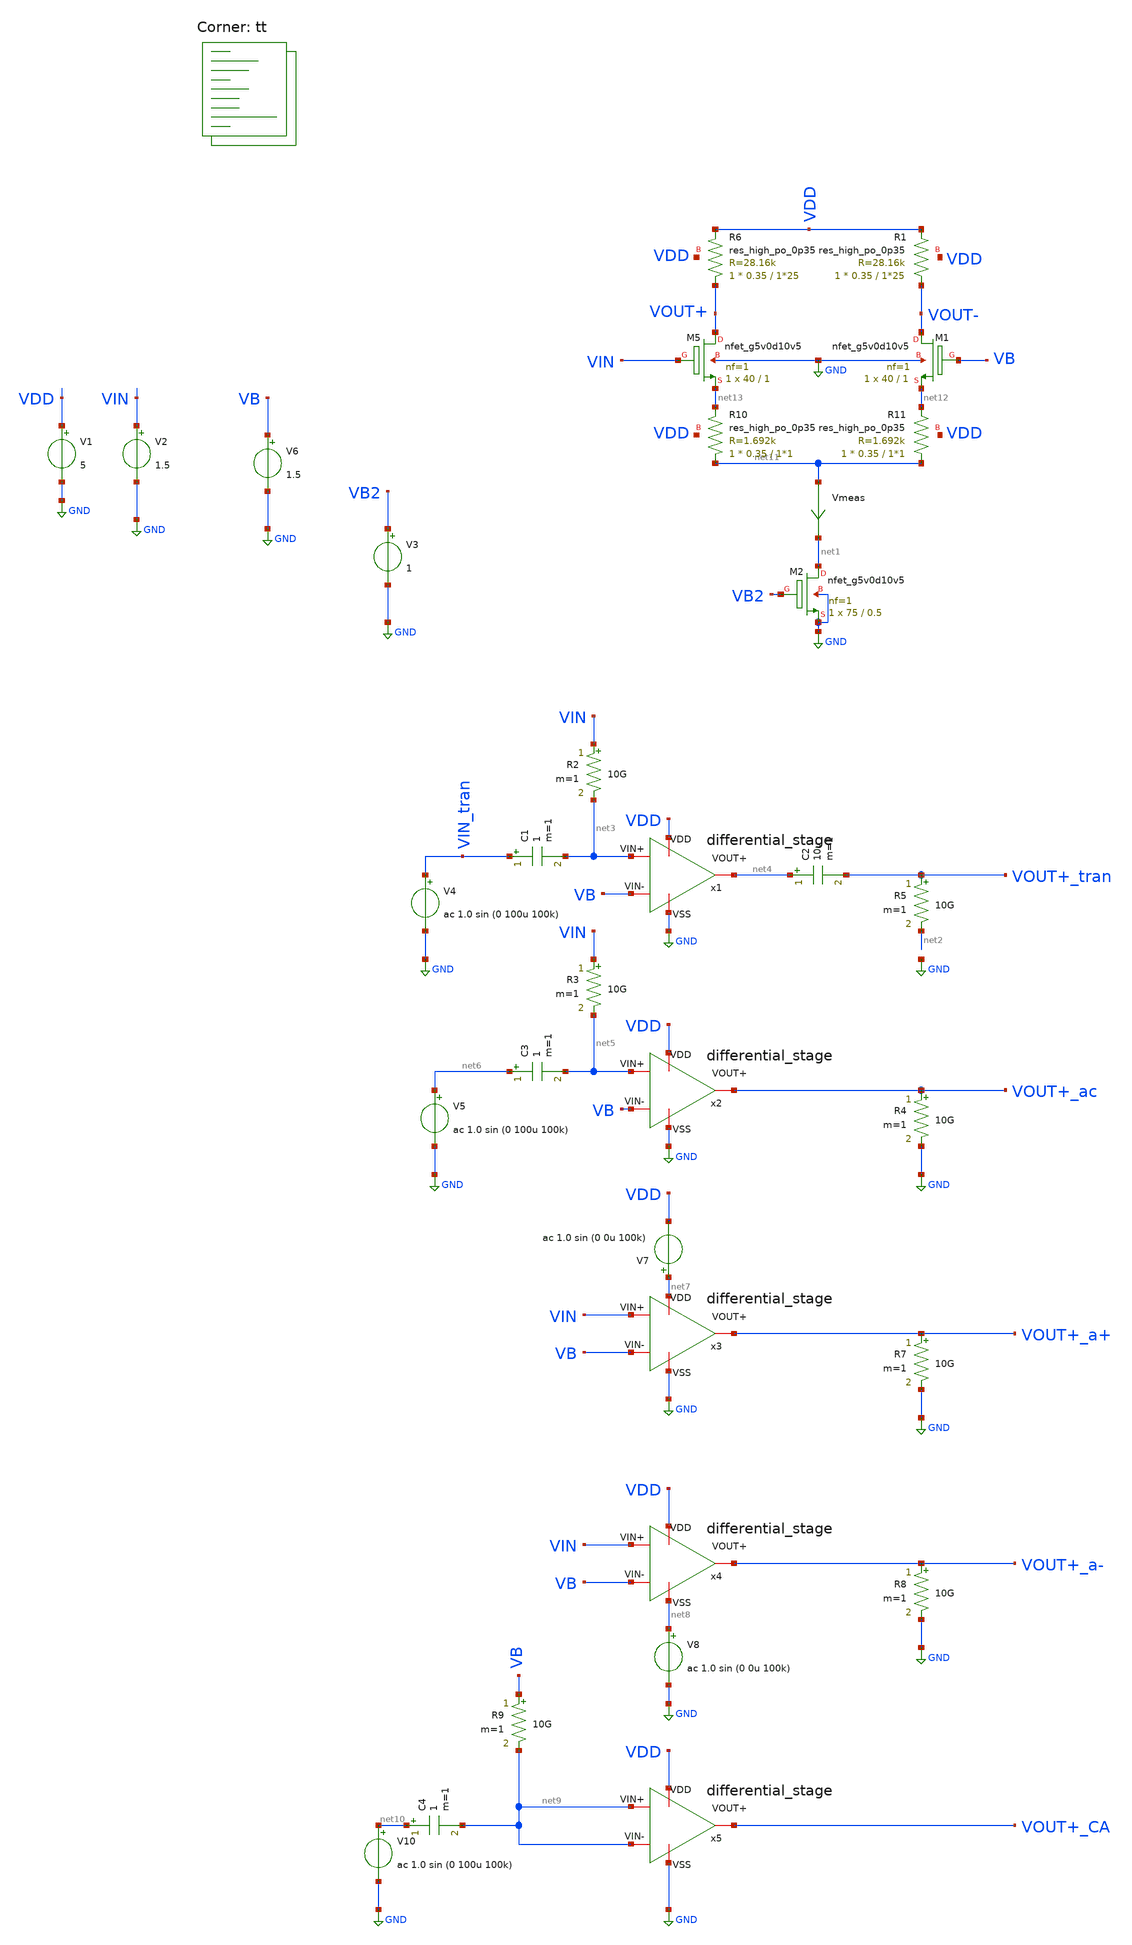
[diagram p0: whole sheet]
** sch_path: amplifiers/differencial_stage_amps/basic_stages/degenerated_stage/diferential_stage.sch
**.subckt diferential_stage
XM5 VOUT+ VIN net13 GND sky130_fd_pr__nfet_g5v0d10v5 L=1 W=40 nf=1 ad='int((1 + 1)/2) * 40 / 1 * 0.29'
+ as='int((1 + 2)/2) * 40 / 1 * 0.29' pd='2*int((1 + 1)/2) * (40 / 1 + 0.29)' ps='2*int((1 + 2)/2) * (40 / 1 + 0.29)'
+ nrd='0.29 / 40 ' nrs='0.29 / 40 ' sa=0 sb=0 sd=0 mult=1 m=1
XM1 VOUT- VB net12 GND sky130_fd_pr__nfet_g5v0d10v5 L=1 W=40 nf=1 ad='int((1 + 1)/2) * 40 / 1 * 0.29'
+ as='int((1 + 2)/2) * 40 / 1 * 0.29' pd='2*int((1 + 1)/2) * (40 / 1 + 0.29)' ps='2*int((1 + 2)/2) * (40 / 1 + 0.29)'
+ nrd='0.29 / 40 ' nrs='0.29 / 40 ' sa=0 sb=0 sd=0 mult=1 m=1
XR6 VOUT+ VDD VDD sky130_fd_pr__res_high_po_0p35 L=1*25 mult=1 m=1
XR1 VOUT- VDD VDD sky130_fd_pr__res_high_po_0p35 L=1*25 mult=1 m=1
V1 VDD GND 5
V2 VIN GND 1.5
V6 VB GND 1.5
XM2 net1 VB2 GND GND sky130_fd_pr__nfet_g5v0d10v5 L=0.5 W=75 nf=1 ad='int((1 + 1)/2) * 75 / 1 * 0.29'
+ as='int((1 + 2)/2) * 75 / 1 * 0.29' pd='2*int((1 + 1)/2) * (75 / 1 + 0.29)' ps='2*int((1 + 2)/2) * (75 / 1 + 0.29)'
+ nrd='0.29 / 75 ' nrs='0.29 / 75 ' sa=0 sb=0 sd=0 mult=1 m=1
V3 VB2 GND 1
Vmeas net11 net1 0
.save i(vmeas)
R5 VOUT+_tran net2 10G m=1
R2 VIN net3 10G m=1
V4 VIN_tran GND ac 1.0 sin (0 100u 100k)
C2 net4 VOUT+_tran 10u m=1
C1 VIN_tran net3 1 m=1
R3 VIN net5 10G m=1
C3 net6 net5 1 m=1
V5 net6 GND ac 1.0 sin (0 100u 100k)
R4 VOUT+_ac GND 10G m=1
V7 net7 VDD ac 1.0 sin (0 0u 100k)
R7 VOUT+_a+ GND 10G m=1
V8 net8 GND ac 1.0 sin (0 0u 100k)
R8 VOUT+_a- GND 10G m=1
R9 VB net9 10G m=1
C4 net10 net9 1 m=1
V10 net10 GND ac 1.0 sin (0 100u 100k)
x1 VDD GND net3 VB net4 differential_stage
x2 VDD GND net5 VB VOUT+_ac differential_stage
x3 net7 GND VIN VB VOUT+_a+ differential_stage
x4 VDD net8 VIN VB VOUT+_a- differential_stage
x5 VDD GND net9 net9 VOUT+_CA differential_stage
XR10 net11 net13 VDD sky130_fd_pr__res_high_po_0p35 L=1*1 mult=1 m=1
XR11 net11 net12 VDD sky130_fd_pr__res_high_po_0p35 L=1*1 mult=1 m=1
**** begin user architecture code

**************************************************************
**************************************************************
**************************************************************
**************************************************************
**************************************************************
*LIBs*********************************************************
**************************************************************
**************************************************************
**************************************************************
**************************************************************
**************************************************************
*.lib $::SKYWATER_MODELS/sky130.lib.spice tt
* chose the corners in the corner file
* tt_mm for mismatch
* ss ff sf fs standart corners
* ll hh lh hl capacitor and resistors corners
* mc for total process variation including corners
**************************************************************
**************************************************************
**************************************************************
**************************************************************
**************************************************************
*Corners/montecarlo options***********************************
**************************************************************
**************************************************************
**************************************************************
**************************************************************
**************************************************************
.TEMP 27
**************************************************************
**************************************************************
**************************************************************
**************************************************************
*SIMULATION and Plots*****************************************
**************************************************************
**************************************************************
**************************************************************
**************************************************************
.control
save all
dc V2 0 5 0.01
*dc simulation
plot v(VOUT-) v(VIN) deriv(v(VOUT-)) v(VOUT+) deriv(v(VOUT+))
*ploting VIN VOUT and the voltage gain
plot i(Vmeas)
*ploting the current for curiosity
tran 0.2ns 20u
*transient simulation
plot (v(VOUT+_tran)) v(VIN_tran)
*simple plot to exemplify the gain
fft v(VOUT+_tran) v(VIN_tran)
*fast fourier transfor
plot mag(v(VOUT+_tran)) mag(v(VIN_tran))
ac dec 20 1 1000G
*simple ac simulation
plot db(v(VOUT+_ac))
plot db(v(VOUT+_a+))
plot db(v(VOUT+_a-))
plot db(v(VOUT+_CA))
plot db((v(VOUT+_ac))/(v(VOUT+_CA)))
plot db((v(VOUT+_ac))/(v(VOUT+_a+)))
plot db((v(VOUT+_ac))/(v(VOUT+_a-)))
.endc

.lib $::SKYWATER_MODELS/sky130.lib.spice tt
**** end user architecture code
**.ends
.GLOBAL GND
.end
